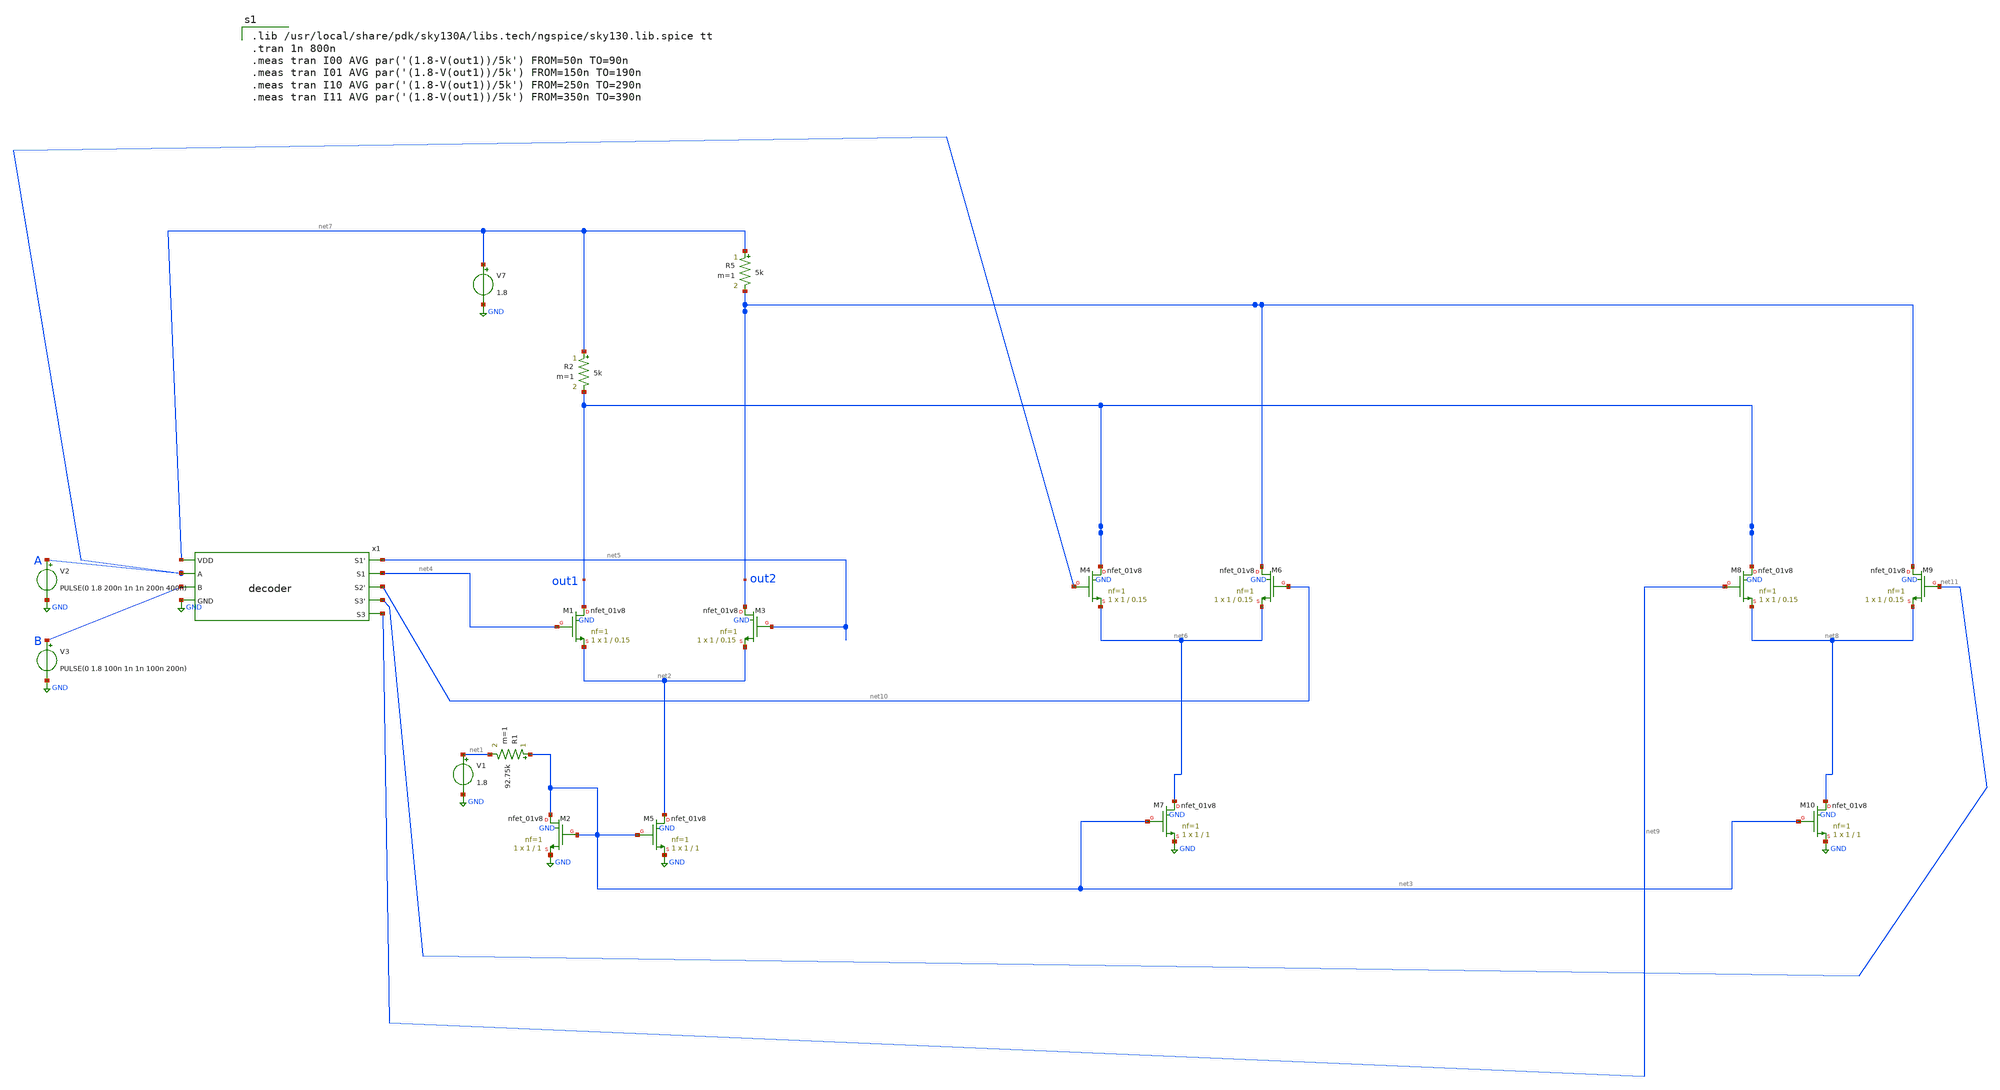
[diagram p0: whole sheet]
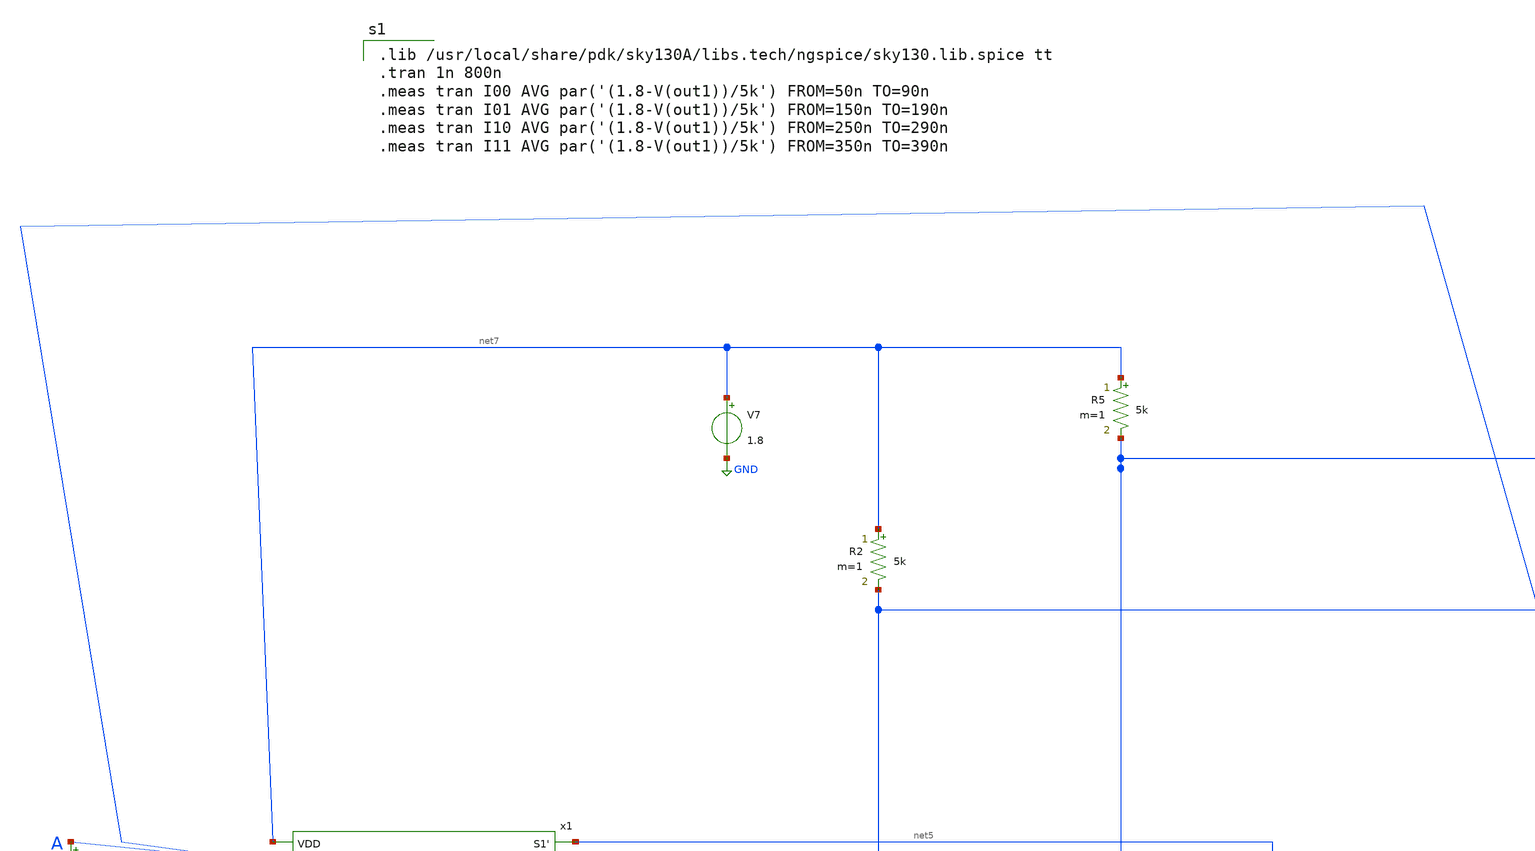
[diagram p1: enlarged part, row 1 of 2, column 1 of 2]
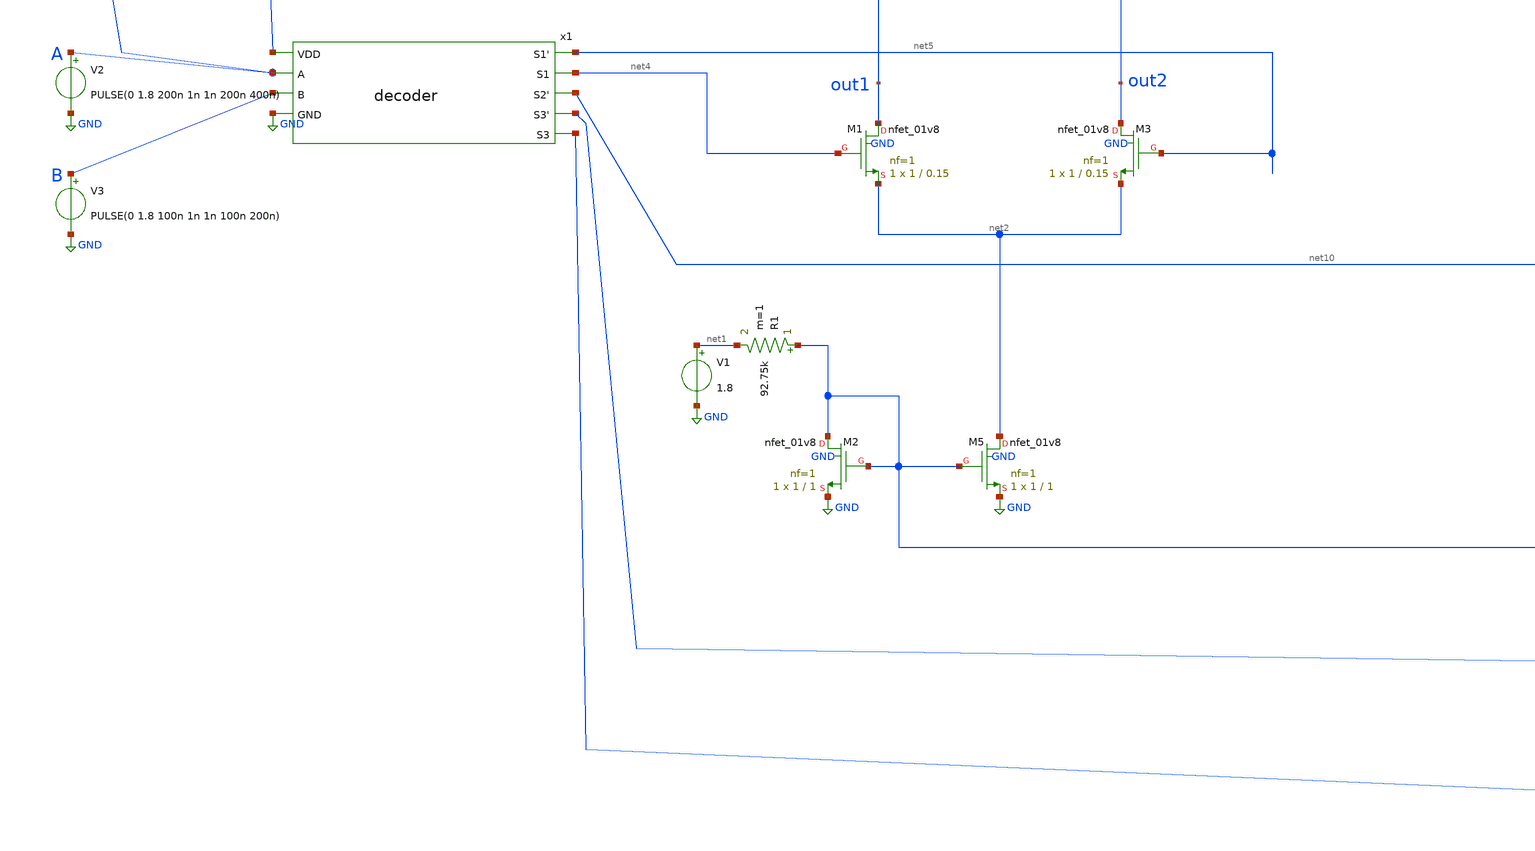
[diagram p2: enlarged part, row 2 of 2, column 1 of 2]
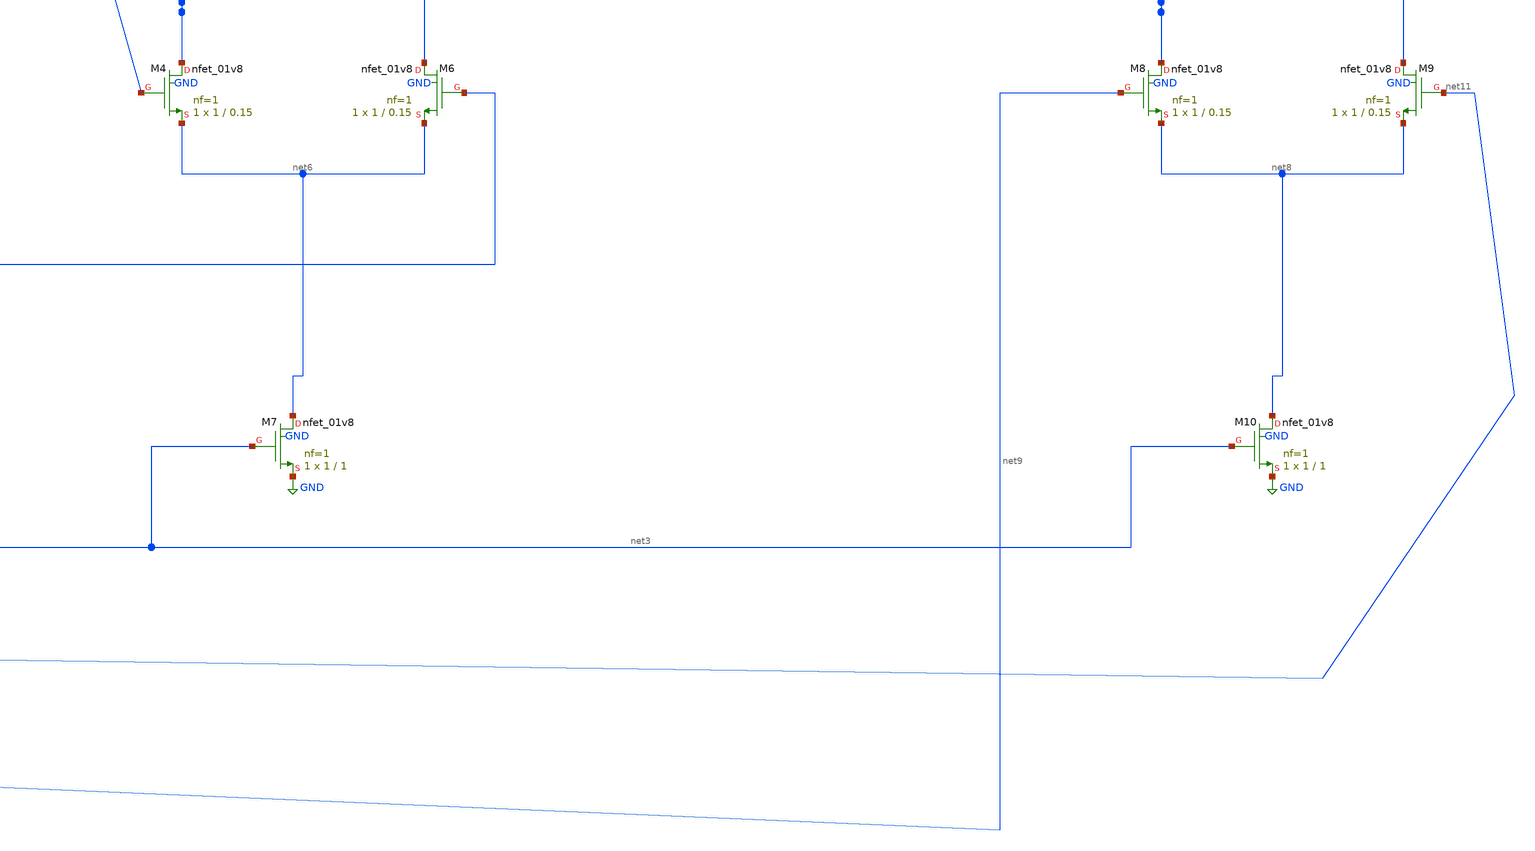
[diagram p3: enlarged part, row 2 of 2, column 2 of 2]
** sch_path: 2_bit_current_steering_DAC/current_steering_dac_2bit.sch
**.subckt current_steering_dac_2bit
XM5 net2 net3 GND GND sky130_fd_pr__nfet_01v8 L=1 W=1 nf=1 ad='int((1 + 1)/2) * 1 / 1 * 0.29' as='int((1 + 2)/2) * 1 / 1 * 0.29'
+ pd='2*int((1 + 1)/2) * (1 / 1 + 0.29)' ps='2*int((1 + 2)/2) * (1 / 1 + 0.29)' nrd='0.29 / 1 ' nrs='0.29 / 1 '
+ sa=0 sb=0 sd=0 mult=1 m=1
XM2 net3 net3 GND GND sky130_fd_pr__nfet_01v8 L=1 W=1 nf=1 ad='int((1 + 1)/2) * 1 / 1 * 0.29' as='int((1 + 2)/2) * 1 / 1 * 0.29'
+ pd='2*int((1 + 1)/2) * (1 / 1 + 0.29)' ps='2*int((1 + 2)/2) * (1 / 1 + 0.29)' nrd='0.29 / 1 ' nrs='0.29 / 1 '
+ sa=0 sb=0 sd=0 mult=1 m=1
V1 net1 GND 1.8
R1 net3 net1 92.75k m=1
XM1 out1 net4 net2 GND sky130_fd_pr__nfet_01v8 L=0.15 W=1 nf=1 ad='int((1 + 1)/2) * 1 / 1 * 0.29' as='int((1 + 2)/2) * 1 / 1 * 0.29'
+ pd='2*int((1 + 1)/2) * (1 / 1 + 0.29)' ps='2*int((1 + 2)/2) * (1 / 1 + 0.29)' nrd='0.29 / 1 ' nrs='0.29 / 1 '
+ sa=0 sb=0 sd=0 mult=1 m=1
XM3 out2 net5 net2 GND sky130_fd_pr__nfet_01v8 L=0.15 W=1 nf=1 ad='int((1 + 1)/2) * 1 / 1 * 0.29' as='int((1 + 2)/2) * 1 / 1 * 0.29'
+ pd='2*int((1 + 1)/2) * (1 / 1 + 0.29)' ps='2*int((1 + 2)/2) * (1 / 1 + 0.29)' nrd='0.29 / 1 ' nrs='0.29 / 1 '
+ sa=0 sb=0 sd=0 mult=1 m=1
XM4 out1 A net6 GND sky130_fd_pr__nfet_01v8 L=0.15 W=1 nf=1 ad='int((1 + 1)/2) * 1 / 1 * 0.29' as='int((1 + 2)/2) * 1 / 1 * 0.29'
+ pd='2*int((1 + 1)/2) * (1 / 1 + 0.29)' ps='2*int((1 + 2)/2) * (1 / 1 + 0.29)' nrd='0.29 / 1 ' nrs='0.29 / 1 '
+ sa=0 sb=0 sd=0 mult=1 m=1
XM6 out2 net10 net6 GND sky130_fd_pr__nfet_01v8 L=0.15 W=1 nf=1 ad='int((1 + 1)/2) * 1 / 1 * 0.29' as='int((1 + 2)/2) * 1 / 1 * 0.29'
+ pd='2*int((1 + 1)/2) * (1 / 1 + 0.29)' ps='2*int((1 + 2)/2) * (1 / 1 + 0.29)' nrd='0.29 / 1 ' nrs='0.29 / 1 '
+ sa=0 sb=0 sd=0 mult=1 m=1
R2 net7 out1 5k m=1
R5 net7 out2 5k m=1
V7 net7 GND 1.8
XM7 net6 net3 GND GND sky130_fd_pr__nfet_01v8 L=1 W=1 nf=1 ad='int((1 + 1)/2) * 1 / 1 * 0.29' as='int((1 + 2)/2) * 1 / 1 * 0.29'
+ pd='2*int((1 + 1)/2) * (1 / 1 + 0.29)' ps='2*int((1 + 2)/2) * (1 / 1 + 0.29)' nrd='0.29 / 1 ' nrs='0.29 / 1 '
+ sa=0 sb=0 sd=0 mult=1 m=1
XM8 out1 net9 net8 GND sky130_fd_pr__nfet_01v8 L=0.15 W=1 nf=1 ad='int((1 + 1)/2) * 1 / 1 * 0.29' as='int((1 + 2)/2) * 1 / 1 * 0.29'
+ pd='2*int((1 + 1)/2) * (1 / 1 + 0.29)' ps='2*int((1 + 2)/2) * (1 / 1 + 0.29)' nrd='0.29 / 1 ' nrs='0.29 / 1 '
+ sa=0 sb=0 sd=0 mult=1 m=1
XM9 out2 net11 net8 GND sky130_fd_pr__nfet_01v8 L=0.15 W=1 nf=1 ad='int((1 + 1)/2) * 1 / 1 * 0.29' as='int((1 + 2)/2) * 1 / 1 * 0.29'
+ pd='2*int((1 + 1)/2) * (1 / 1 + 0.29)' ps='2*int((1 + 2)/2) * (1 / 1 + 0.29)' nrd='0.29 / 1 ' nrs='0.29 / 1 '
+ sa=0 sb=0 sd=0 mult=1 m=1
XM10 net8 net3 GND GND sky130_fd_pr__nfet_01v8 L=1 W=1 nf=1 ad='int((1 + 1)/2) * 1 / 1 * 0.29' as='int((1 + 2)/2) * 1 / 1 * 0.29'
+ pd='2*int((1 + 1)/2) * (1 / 1 + 0.29)' ps='2*int((1 + 2)/2) * (1 / 1 + 0.29)' nrd='0.29 / 1 ' nrs='0.29 / 1 '
+ sa=0 sb=0 sd=0 mult=1 m=1
V2 A GND PULSE(0 1.8 200n 1n 1n 200n 400n)
V3 B GND PULSE(0 1.8 100n 1n 1n 100n 200n)
x1 net7 A B net5 net4 net10 net11 net9 GND decoder
**** begin user architecture code

.lib /usr/local/share/pdk/sky130A/libs.tech/ngspice/sky130.lib.spice tt
.tran 1n 800n
.meas tran I00 AVG par('(1.8-V(out1))/5k') FROM=50n TO=90n
.meas tran I01 AVG par('(1.8-V(out1))/5k') FROM=150n TO=190n
.meas tran I10 AVG par('(1.8-V(out1))/5k') FROM=250n TO=290n
.meas tran I11 AVG par('(1.8-V(out1))/5k') FROM=350n TO=390n

**** end user architecture code
**.ends

* expanding   symbol:  decoder.sym # of pins=9
** sym_path: 2_bit_current_steering_DAC/decoder.sym
** sch_path: 2_bit_current_steering_DAC/decoder.sch
.subckt decoder VDD A B S1' S1 S2' S3' S3 GND
*.ipin A
*.ipin B
*.ipin VDD
*.ipin GND
*.opin S1'
*.opin S1
*.opin S2'
*.opin S3
*.opin S3'
x3 VDD A S1' B GND nor
x1 VDD S1' S1 GND inverter
x4 VDD A S2' GND inverter
x6 VDD A S3' B GND nand
x2 VDD S3' S3 GND inverter
.ends


* expanding   symbol:  nor.sym # of pins=5
** sym_path: 2_bit_current_steering_DAC/nor.sym
** sch_path: 2_bit_current_steering_DAC/nor.sch
.subckt nor VDD B out A VSS
*.ipin A
*.ipin B
*.ipin VDD
*.ipin VSS
*.opin out
XM1 out A VSS GND sky130_fd_pr__nfet_01v8 L=0.15 W=1 nf=1 ad='int((1 + 1)/2) * 1 / 1 * 0.29' as='int((1
+ + 2)/2) * 1 / 1 * 0.29' pd='2*int((1 + 1)/2) * (1 / 1 + 0.29)' ps='2*int((1 + 2)/2) * (1 / 1 + 0.29)' nrd='0.29
+ / 1 ' nrs='0.29 / 1 ' sa=0 sb=0 sd=0 mult=1 m=1
XM3 out B VSS GND sky130_fd_pr__nfet_01v8 L=0.15 W=1 nf=1 ad='int((1 + 1)/2) * 1 / 1 * 0.29' as='int((1
+ + 2)/2) * 1 / 1 * 0.29' pd='2*int((1 + 1)/2) * (1 / 1 + 0.29)' ps='2*int((1 + 2)/2) * (1 / 1 + 0.29)' nrd='0.29
+ / 1 ' nrs='0.29 / 1 ' sa=0 sb=0 sd=0 mult=1 m=1
XM2 out A net1 VDD sky130_fd_pr__pfet_01v8 L=0.15 W=1 nf=1 ad='int((1 + 1)/2) * 1 / 1 * 0.29' as='int((1
+ + 2)/2) * 1 / 1 * 0.29' pd='2*int((1 + 1)/2) * (1 / 1 + 0.29)' ps='2*int((1 + 2)/2) * (1 / 1 + 0.29)' nrd='0.29
+ / 1 ' nrs='0.29 / 1 ' sa=0 sb=0 sd=0 mult=1 m=1
XM4 net1 B VDD VDD sky130_fd_pr__pfet_01v8 L=0.15 W=1 nf=1 ad='int((1 + 1)/2) * 1 / 1 * 0.29' as='int((1
+ + 2)/2) * 1 / 1 * 0.29' pd='2*int((1 + 1)/2) * (1 / 1 + 0.29)' ps='2*int((1 + 2)/2) * (1 / 1 + 0.29)' nrd='0.29
+ / 1 ' nrs='0.29 / 1 ' sa=0 sb=0 sd=0 mult=1 m=1
.ends


* expanding   symbol:  inverter.sym # of pins=4
** sym_path: 2_bit_current_steering_DAC/inverter.sym
** sch_path: 2_bit_current_steering_DAC/inverter.sch
.subckt inverter VDD Vin Vout VSS
*.ipin VDD
*.ipin Vin
*.ipin VSS
*.opin Vout
XM1 Vout Vin VSS GND sky130_fd_pr__nfet_01v8 L=0.15 W=1 nf=1 ad='int((1 + 1)/2) * 1 / 1 * 0.29' as='int((1
+ + 2)/2) * 1 / 1 * 0.29' pd='2*int((1 + 1)/2) * (1 / 1 + 0.29)' ps='2*int((1 + 2)/2) * (1 / 1 + 0.29)' nrd='0.29
+ / 1 ' nrs='0.29 / 1 ' sa=0 sb=0 sd=0 mult=1 m=1
XM2 Vout Vin VDD VDD sky130_fd_pr__pfet_01v8 L=0.15 W=1 nf=1 ad='int((1 + 1)/2) * 1 / 1 * 0.29' as='int((1
+ + 2)/2) * 1 / 1 * 0.29' pd='2*int((1 + 1)/2) * (1 / 1 + 0.29)' ps='2*int((1 + 2)/2) * (1 / 1 + 0.29)' nrd='0.29
+ / 1 ' nrs='0.29 / 1 ' sa=0 sb=0 sd=0 mult=1 m=1
.ends


* expanding   symbol:  nand.sym # of pins=5
** sym_path: 2_bit_current_steering_DAC/nand.sym
** sch_path: 2_bit_current_steering_DAC/nand.sch
.subckt nand VDD A out B VSS
*.ipin A
*.ipin VDD
*.ipin B
*.ipin VSS
*.opin out
XM1 net1 B VSS GND sky130_fd_pr__nfet_01v8 L=0.15 W=1 nf=1 ad='int((1 + 1)/2) * 1 / 1 * 0.29' as='int((1
+ + 2)/2) * 1 / 1 * 0.29' pd='2*int((1 + 1)/2) * (1 / 1 + 0.29)' ps='2*int((1 + 2)/2) * (1 / 1 + 0.29)' nrd='0.29
+ / 1 ' nrs='0.29 / 1 ' sa=0 sb=0 sd=0 mult=1 m=1
XM2 out A net1 GND sky130_fd_pr__nfet_01v8 L=0.15 W=1 nf=1 ad='int((1 + 1)/2) * 1 / 1 * 0.29' as='int((1
+ + 2)/2) * 1 / 1 * 0.29' pd='2*int((1 + 1)/2) * (1 / 1 + 0.29)' ps='2*int((1 + 2)/2) * (1 / 1 + 0.29)' nrd='0.29
+ / 1 ' nrs='0.29 / 1 ' sa=0 sb=0 sd=0 mult=1 m=1
XM3 out A VDD VDD sky130_fd_pr__pfet_01v8 L=0.15 W=1 nf=1 ad='int((1 + 1)/2) * 1 / 1 * 0.29' as='int((1
+ + 2)/2) * 1 / 1 * 0.29' pd='2*int((1 + 1)/2) * (1 / 1 + 0.29)' ps='2*int((1 + 2)/2) * (1 / 1 + 0.29)' nrd='0.29
+ / 1 ' nrs='0.29 / 1 ' sa=0 sb=0 sd=0 mult=1 m=1
XM4 out B VDD VDD sky130_fd_pr__pfet_01v8 L=0.15 W=1 nf=1 ad='int((1 + 1)/2) * 1 / 1 * 0.29' as='int((1
+ + 2)/2) * 1 / 1 * 0.29' pd='2*int((1 + 1)/2) * (1 / 1 + 0.29)' ps='2*int((1 + 2)/2) * (1 / 1 + 0.29)' nrd='0.29
+ / 1 ' nrs='0.29 / 1 ' sa=0 sb=0 sd=0 mult=1 m=1
.ends

.GLOBAL GND
.end
